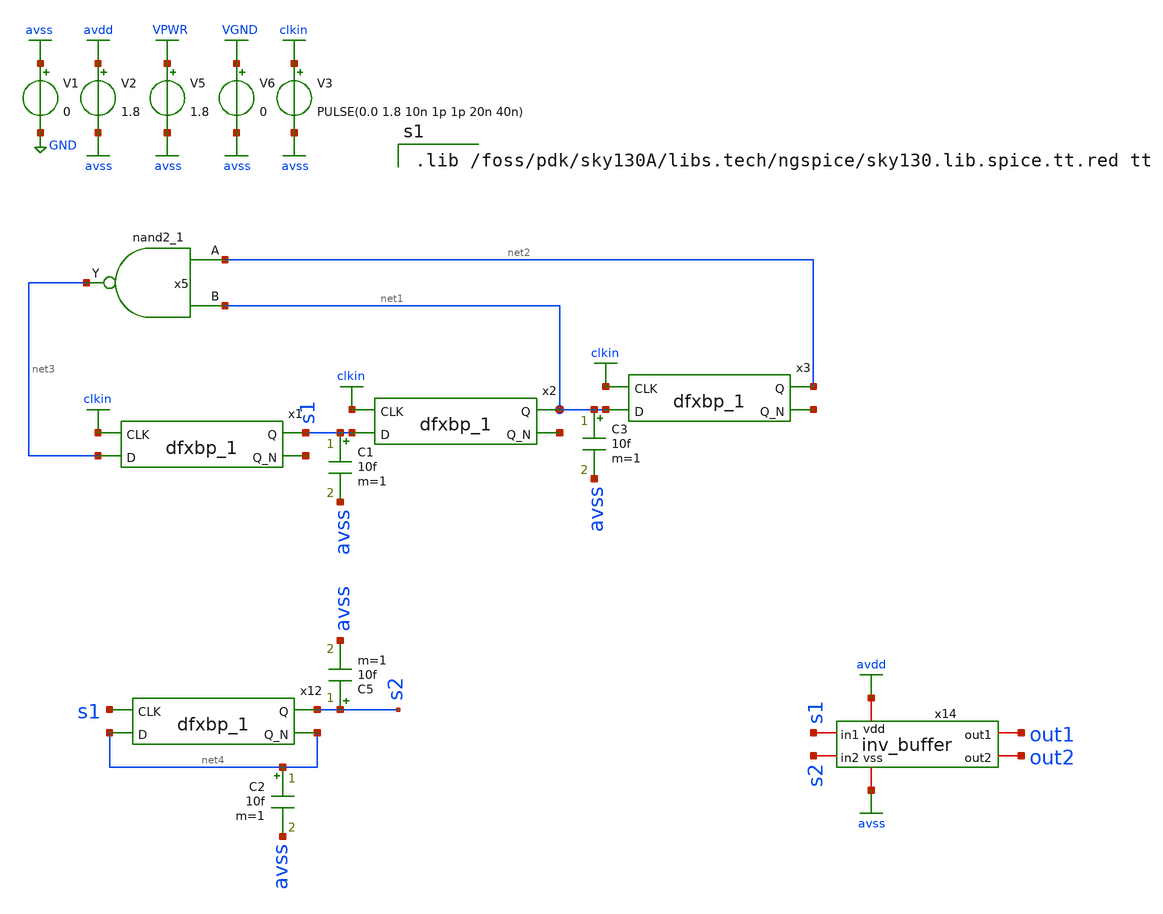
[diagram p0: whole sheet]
** sch_path: xschem/delayflop_2.sch
**.subckt delayflop_2
x1 clkin net3 VGND VNB VPB VPWR s1 net5 sky130_fd_sc_hd__dfxbp_1
V1 avss GND 0
V2 avdd avss 1.8
x2 clkin s1 VGND VNB VPB VPWR net1 net6 sky130_fd_sc_hd__dfxbp_1
V3 clkin avss PULSE(0.0 1.8 10n 1p 1p 20n 40n)
V5 VPWR avss 1.8
V6 VGND avss 0
C1 s1 avss 10f m=1
x3 clkin net1 VGND VNB VPB VPWR net2 net7 sky130_fd_sc_hd__dfxbp_1
x5 net2 net1 VGND VNB VPB VPWR net3 sky130_fd_sc_hd__nand2_1
C3 net1 avss 10f m=1
x12 s1 net4 VGND VNB VPB VPWR s2 net4 sky130_fd_sc_hd__dfxbp_1
C2 net4 avss 10f m=1
C5 s2 avss 10f m=1
x14 avdd avss out1 out2 s2 s1 inv_buffer
**** begin user architecture code

.lib /foss/pdk/sky130A/libs.tech/ngspice/sky130.lib.spice.tt.red tt



.include /foss/pdk/sky130A/libs.ref/sky130_fd_sc_hd/spice/sky130_fd_sc_hd.spice
.control
set temp=25
save clkin din s1 s2 out1 out2 @V1[i]
tran 0.01n 2000n 0n
*plot @V1[i]
*plot clkin din s1 s2 out1 xlimit 500ns 10ns
*plot clkin s1 s2
*plot clkin s1 s2
plot clkin s2
fft clkin s1 s2
*plot db(mag(out1)) xlimit 0.1g 15g ylimit 0.0 -200
*plot db(mag(clk)) xlimit 0.1g 15g ylimit 0.0 -200
plot db(mag(clkin)) db(mag(s1)) db(mag(s2)) xlimit 0.0meg 50meg ylimit 0.0 -200
.endc
.end


**** end user architecture code
**.ends

* expanding   symbol:  ma2022/inv_buffer.sym # of pins=6
** sym_path: xschem/inv_buffer.sym
** sch_path: xschem/inv_buffer.sch
.subckt inv_buffer vdd vss out1 out2 in2 in1
*.iopin in1
*.iopin in2
*.iopin out1
*.iopin out2
*.iopin vdd
*.iopin vss
XM6 net1 in2 vss vss sky130_fd_pr__nfet_01v8 L=0.15 W=0.7 nf=1 ad='int((nf+1)/2) * W/nf * 0.29' as='int((nf+2)/2) * W/nf * 0.29'
+ pd='2*int((nf+1)/2) * (W/nf + 0.29)' ps='2*int((nf+2)/2) * (W/nf + 0.29)' nrd='0.29 / W' nrs='0.29 / W'
+ sa=0 sb=0 sd=0 mult=1 m=1
XM8 net2 in1 vss vss sky130_fd_pr__nfet_01v8 L=0.15 W=0.7 nf=1 ad='int((nf+1)/2) * W/nf * 0.29' as='int((nf+2)/2) * W/nf * 0.29'
+ pd='2*int((nf+1)/2) * (W/nf + 0.29)' ps='2*int((nf+2)/2) * (W/nf + 0.29)' nrd='0.29 / W' nrs='0.29 / W'
+ sa=0 sb=0 sd=0 mult=1 m=1
XM9 net2 in1 vdd vdd sky130_fd_pr__pfet_01v8 L=0.15 W=1.4 nf=1 ad='int((nf+1)/2) * W/nf * 0.29' as='int((nf+2)/2) * W/nf * 0.29'
+ pd='2*int((nf+1)/2) * (W/nf + 0.29)' ps='2*int((nf+2)/2) * (W/nf + 0.29)' nrd='0.29 / W' nrs='0.29 / W'
+ sa=0 sb=0 sd=0 mult=1 m=1
XM4 out1 net2 vss vss sky130_fd_pr__nfet_01v8 L=0.15 W=0.7 nf=1 ad='int((nf+1)/2) * W/nf * 0.29' as='int((nf+2)/2) * W/nf * 0.29'
+ pd='2*int((nf+1)/2) * (W/nf + 0.29)' ps='2*int((nf+2)/2) * (W/nf + 0.29)' nrd='0.29 / W' nrs='0.29 / W'
+ sa=0 sb=0 sd=0 mult=1 m=1
XM10 out2 net1 vss vss sky130_fd_pr__nfet_01v8 L=0.15 W=0.7 nf=1 ad='int((nf+1)/2) * W/nf * 0.29' as='int((nf+2)/2) * W/nf * 0.29'
+ pd='2*int((nf+1)/2) * (W/nf + 0.29)' ps='2*int((nf+2)/2) * (W/nf + 0.29)' nrd='0.29 / W' nrs='0.29 / W'
+ sa=0 sb=0 sd=0 mult=1 m=1
XM1 out1 net2 vdd vdd sky130_fd_pr__pfet_01v8 L=0.15 W=1.4 nf=1 ad='int((nf+1)/2) * W/nf * 0.29' as='int((nf+2)/2) * W/nf * 0.29'
+ pd='2*int((nf+1)/2) * (W/nf + 0.29)' ps='2*int((nf+2)/2) * (W/nf + 0.29)' nrd='0.29 / W' nrs='0.29 / W'
+ sa=0 sb=0 sd=0 mult=1 m=1
XM2 net1 in2 vdd vdd sky130_fd_pr__pfet_01v8 L=0.15 W=1.4 nf=1 ad='int((nf+1)/2) * W/nf * 0.29' as='int((nf+2)/2) * W/nf * 0.29'
+ pd='2*int((nf+1)/2) * (W/nf + 0.29)' ps='2*int((nf+2)/2) * (W/nf + 0.29)' nrd='0.29 / W' nrs='0.29 / W'
+ sa=0 sb=0 sd=0 mult=1 m=1
XM3 out2 net1 vdd vdd sky130_fd_pr__pfet_01v8 L=0.15 W=1.4 nf=1 ad='int((nf+1)/2) * W/nf * 0.29' as='int((nf+2)/2) * W/nf * 0.29'
+ pd='2*int((nf+1)/2) * (W/nf + 0.29)' ps='2*int((nf+2)/2) * (W/nf + 0.29)' nrd='0.29 / W' nrs='0.29 / W'
+ sa=0 sb=0 sd=0 mult=1 m=1
.ends

.GLOBAL avdd
.GLOBAL avss
.GLOBAL GND
.GLOBAL clkin
.GLOBAL VPWR
.GLOBAL VGND
.end
